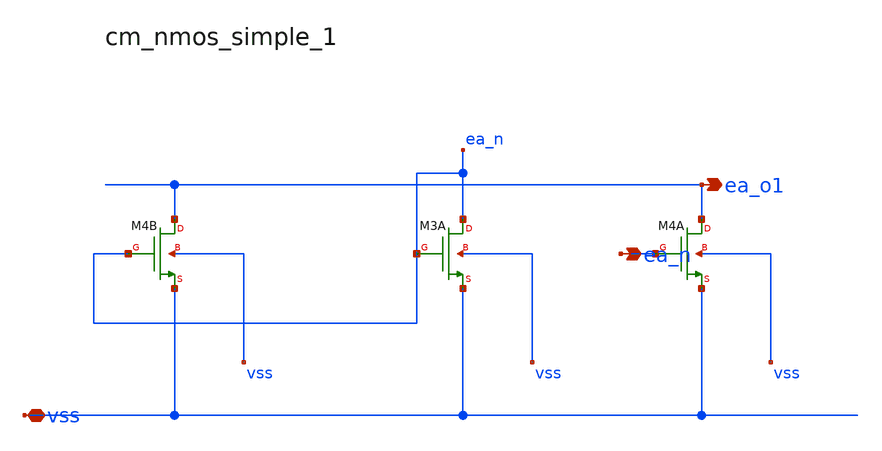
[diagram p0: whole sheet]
** sch_path: analog-db/raw/ldo_010_capless_lowiq/hier/blocks/cm_nmos_simple_1.sch
**.subckt cm_nmos_simple_1 vss ea_o1 ea_n
*.iopin vss
*.opin ea_o1
*.opin ea_n
XM3A ea_n ea_n vss vss sg13_lv_nmos w={x_dut_xm3_w/2} l=x_dut_xm3_l ng=1 m=1
XM4A ea_o1 ea_n vss vss sg13_lv_nmos w={x_dut_xm3_w/2} l=x_dut_xm3_l ng=1 m=1
XM4B ea_o1 ea_n vss vss sg13_lv_nmos w={x_dut_xm3_w/2} l=x_dut_xm3_l ng=1 m=1
**.ends
.end
